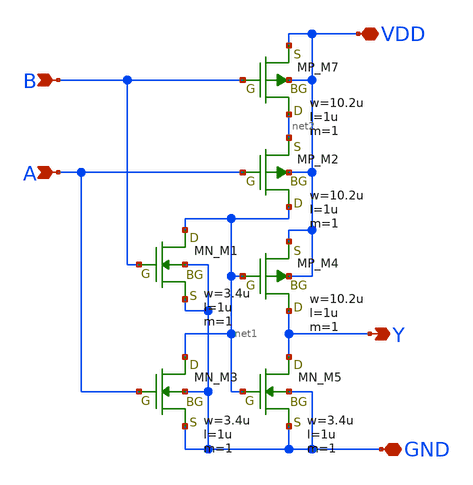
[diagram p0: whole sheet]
** sch_path: libs.tech/xschem/TR-1um_5_stdcell/OR2.sch
**.subckt OR2 A B Y VDD GND
*.ipin A
*.ipin B
*.opin Y
*.iopin VDD
*.iopin GND
XM7 net2 B VDD VDD PMOS w=10.2u l=1u nrd=0 nrs=0 m=1
XM2 net1 A net2 VDD PMOS w=10.2u l=1u nrd=0 nrs=0 m=1
XM4 Y net1 VDD VDD PMOS w=10.2u l=1u nrd=0 nrs=0 m=1
XM1 net1 B GND GND NMOS w=3.4u l=1u nrd=0 nrs=0 m=1
XM3 net1 A GND GND NMOS w=3.4u l=1u nrd=0 nrs=0 m=1
XM5 Y net1 GND GND NMOS w=3.4u l=1u nrd=0 nrs=0 m=1
**.ends
.end
